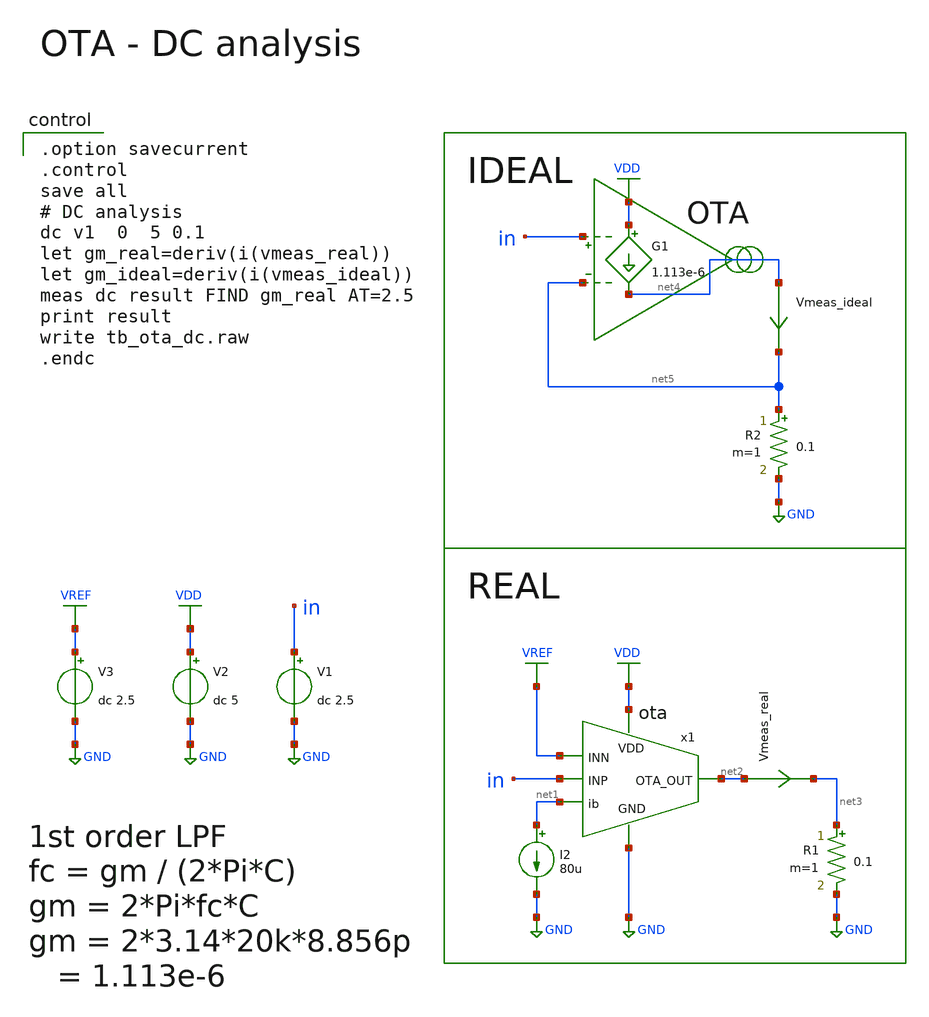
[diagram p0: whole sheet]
** sch_path: member_project/AM_Radio/Yamada3/xschem/tb_ota_dc.sch
**.subckt tb_ota_dc
V2 VDD GND dc 5
V1 in GND dc 2.5
x1 VDD net1 VREF in net2 GND ota
I2 net1 GND 80u
Vmeas_real net2 net3 0
.save i(vmeas_real)
R1 net3 GND 0.1 m=1
V3 VREF GND dc 2.5
G1 VDD net4 in net5 1.113e-6
R2 net5 GND 0.1 m=1
Vmeas_ideal net4 net5 0
.save i(vmeas_ideal)
**** begin user architecture code

.option savecurrent
.control
save all
# DC analysis
dc v1  0  5 0.1
let gm_real=deriv(i(vmeas_real))
let gm_ideal=deriv(i(vmeas_ideal))
meas dc result FIND gm_real AT=2.5
print result
write tb_ota_dc.raw
.endc

 .include $::LIB/ip62_models
**** end user architecture code
**.ends
.GLOBAL GND
.GLOBAL VDD
.GLOBAL VREF
.end
